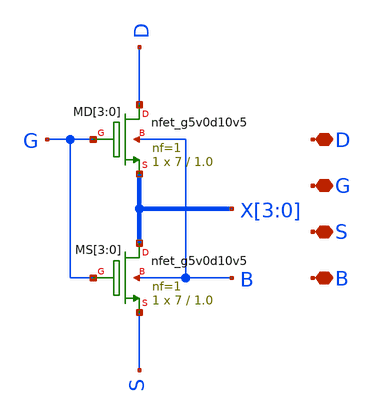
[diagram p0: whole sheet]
** sch_path: xschem/n1_1.sch
**.subckt n1_1 D G S B
*.iopin D
*.iopin G
*.iopin S
*.iopin B
XMD[3] D G X[3] B sky130_fd_pr__nfet_g5v0d10v5 L=1.0 W=7 nf=1 ad='int((nf+1)/2) * W/nf * 0.29' as='int((nf+2)/2) * W/nf * 0.29'
+ pd='2*int((nf+1)/2) * (W/nf + 0.29)' ps='2*int((nf+2)/2) * (W/nf + 0.29)' nrd='0.29 / W' nrs='0.29 / W'
+ sa=0 sb=0 sd=0 mult=1 m=1
XMD[2] D G X[2] B sky130_fd_pr__nfet_g5v0d10v5 L=1.0 W=7 nf=1 ad='int((nf+1)/2) * W/nf * 0.29' as='int((nf+2)/2) * W/nf * 0.29'
+ pd='2*int((nf+1)/2) * (W/nf + 0.29)' ps='2*int((nf+2)/2) * (W/nf + 0.29)' nrd='0.29 / W' nrs='0.29 / W'
+ sa=0 sb=0 sd=0 mult=1 m=1
XMD[1] D G X[1] B sky130_fd_pr__nfet_g5v0d10v5 L=1.0 W=7 nf=1 ad='int((nf+1)/2) * W/nf * 0.29' as='int((nf+2)/2) * W/nf * 0.29'
+ pd='2*int((nf+1)/2) * (W/nf + 0.29)' ps='2*int((nf+2)/2) * (W/nf + 0.29)' nrd='0.29 / W' nrs='0.29 / W'
+ sa=0 sb=0 sd=0 mult=1 m=1
XMD[0] D G X[0] B sky130_fd_pr__nfet_g5v0d10v5 L=1.0 W=7 nf=1 ad='int((nf+1)/2) * W/nf * 0.29' as='int((nf+2)/2) * W/nf * 0.29'
+ pd='2*int((nf+1)/2) * (W/nf + 0.29)' ps='2*int((nf+2)/2) * (W/nf + 0.29)' nrd='0.29 / W' nrs='0.29 / W'
+ sa=0 sb=0 sd=0 mult=1 m=1
XMS[3] X[3] G S B sky130_fd_pr__nfet_g5v0d10v5 L=1.0 W=7 nf=1 ad='int((nf+1)/2) * W/nf * 0.29' as='int((nf+2)/2) * W/nf * 0.29'
+ pd='2*int((nf+1)/2) * (W/nf + 0.29)' ps='2*int((nf+2)/2) * (W/nf + 0.29)' nrd='0.29 / W' nrs='0.29 / W'
+ sa=0 sb=0 sd=0 mult=1 m=1
XMS[2] X[2] G S B sky130_fd_pr__nfet_g5v0d10v5 L=1.0 W=7 nf=1 ad='int((nf+1)/2) * W/nf * 0.29' as='int((nf+2)/2) * W/nf * 0.29'
+ pd='2*int((nf+1)/2) * (W/nf + 0.29)' ps='2*int((nf+2)/2) * (W/nf + 0.29)' nrd='0.29 / W' nrs='0.29 / W'
+ sa=0 sb=0 sd=0 mult=1 m=1
XMS[1] X[1] G S B sky130_fd_pr__nfet_g5v0d10v5 L=1.0 W=7 nf=1 ad='int((nf+1)/2) * W/nf * 0.29' as='int((nf+2)/2) * W/nf * 0.29'
+ pd='2*int((nf+1)/2) * (W/nf + 0.29)' ps='2*int((nf+2)/2) * (W/nf + 0.29)' nrd='0.29 / W' nrs='0.29 / W'
+ sa=0 sb=0 sd=0 mult=1 m=1
XMS[0] X[0] G S B sky130_fd_pr__nfet_g5v0d10v5 L=1.0 W=7 nf=1 ad='int((nf+1)/2) * W/nf * 0.29' as='int((nf+2)/2) * W/nf * 0.29'
+ pd='2*int((nf+1)/2) * (W/nf + 0.29)' ps='2*int((nf+2)/2) * (W/nf + 0.29)' nrd='0.29 / W' nrs='0.29 / W'
+ sa=0 sb=0 sd=0 mult=1 m=1
**.ends
.end
